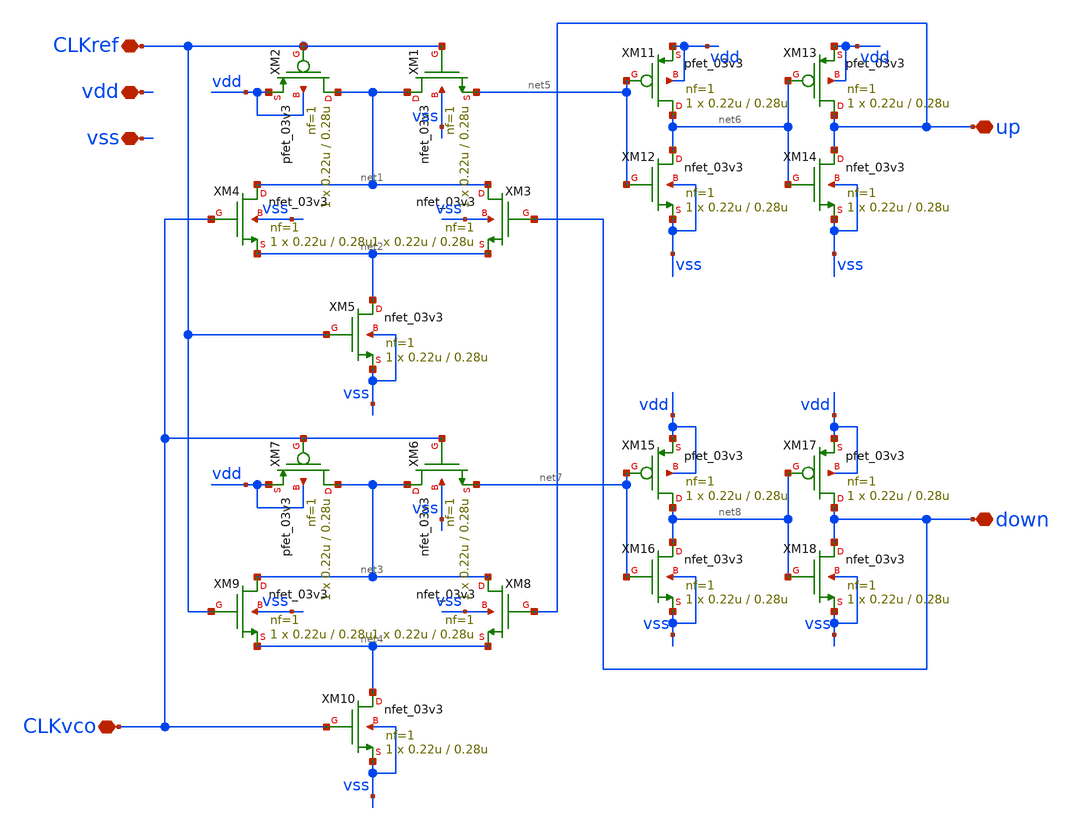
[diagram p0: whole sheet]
** sch_path: designs/libs/qw_core_analog_pkedit/untitled-1.sch
**.subckt untitled-1 CLKref CLKvco vdd vss up down
*.iopin CLKref
*.iopin CLKvco
*.iopin vdd
*.iopin vss
*.iopin up
*.iopin down
XM1 net1 CLKref net5 vss nfet_03v3 L=0.28u W=0.22u nf=1 ad='int((nf+1)/2) * W/nf * 0.18u' as='int((nf+2)/2) * W/nf * 0.18u'
+ pd='2*int((nf+1)/2) * (W/nf + 0.18u)' ps='2*int((nf+2)/2) * (W/nf + 0.18u)' nrd='0.18u / W' nrs='0.18u / W'
+ sa=0 sb=0 sd=0 m=1
XM2 net1 CLKref vdd vdd pfet_03v3 L=0.28u W=0.22u nf=1 ad='int((nf+1)/2) * W/nf * 0.18u' as='int((nf+2)/2) * W/nf * 0.18u'
+ pd='2*int((nf+1)/2) * (W/nf + 0.18u)' ps='2*int((nf+2)/2) * (W/nf + 0.18u)' nrd='0.18u / W' nrs='0.18u / W'
+ sa=0 sb=0 sd=0 m=1
XM3 net1 down net2 vss nfet_03v3 L=0.28u W=0.22u nf=1 ad='int((nf+1)/2) * W/nf * 0.18u' as='int((nf+2)/2) * W/nf * 0.18u'
+ pd='2*int((nf+1)/2) * (W/nf + 0.18u)' ps='2*int((nf+2)/2) * (W/nf + 0.18u)' nrd='0.18u / W' nrs='0.18u / W'
+ sa=0 sb=0 sd=0 m=1
XM4 net1 CLKvco net2 vss nfet_03v3 L=0.28u W=0.22u nf=1 ad='int((nf+1)/2) * W/nf * 0.18u' as='int((nf+2)/2) * W/nf * 0.18u'
+ pd='2*int((nf+1)/2) * (W/nf + 0.18u)' ps='2*int((nf+2)/2) * (W/nf + 0.18u)' nrd='0.18u / W' nrs='0.18u / W'
+ sa=0 sb=0 sd=0 m=1
XM5 net2 CLKref vss vss nfet_03v3 L=0.28u W=0.22u nf=1 ad='int((nf+1)/2) * W/nf * 0.18u' as='int((nf+2)/2) * W/nf * 0.18u'
+ pd='2*int((nf+1)/2) * (W/nf + 0.18u)' ps='2*int((nf+2)/2) * (W/nf + 0.18u)' nrd='0.18u / W' nrs='0.18u / W'
+ sa=0 sb=0 sd=0 m=1
XM6 net3 CLKvco net7 vss nfet_03v3 L=0.28u W=0.22u nf=1 ad='int((nf+1)/2) * W/nf * 0.18u' as='int((nf+2)/2) * W/nf * 0.18u'
+ pd='2*int((nf+1)/2) * (W/nf + 0.18u)' ps='2*int((nf+2)/2) * (W/nf + 0.18u)' nrd='0.18u / W' nrs='0.18u / W'
+ sa=0 sb=0 sd=0 m=1
XM7 net3 CLKvco vdd vdd pfet_03v3 L=0.28u W=0.22u nf=1 ad='int((nf+1)/2) * W/nf * 0.18u' as='int((nf+2)/2) * W/nf * 0.18u'
+ pd='2*int((nf+1)/2) * (W/nf + 0.18u)' ps='2*int((nf+2)/2) * (W/nf + 0.18u)' nrd='0.18u / W' nrs='0.18u / W'
+ sa=0 sb=0 sd=0 m=1
XM8 net3 up net4 vss nfet_03v3 L=0.28u W=0.22u nf=1 ad='int((nf+1)/2) * W/nf * 0.18u' as='int((nf+2)/2) * W/nf * 0.18u'
+ pd='2*int((nf+1)/2) * (W/nf + 0.18u)' ps='2*int((nf+2)/2) * (W/nf + 0.18u)' nrd='0.18u / W' nrs='0.18u / W'
+ sa=0 sb=0 sd=0 m=1
XM9 net3 CLKref net4 vss nfet_03v3 L=0.28u W=0.22u nf=1 ad='int((nf+1)/2) * W/nf * 0.18u' as='int((nf+2)/2) * W/nf * 0.18u'
+ pd='2*int((nf+1)/2) * (W/nf + 0.18u)' ps='2*int((nf+2)/2) * (W/nf + 0.18u)' nrd='0.18u / W' nrs='0.18u / W'
+ sa=0 sb=0 sd=0 m=1
XM10 net4 CLKvco vss vss nfet_03v3 L=0.28u W=0.22u nf=1 ad='int((nf+1)/2) * W/nf * 0.18u' as='int((nf+2)/2) * W/nf * 0.18u'
+ pd='2*int((nf+1)/2) * (W/nf + 0.18u)' ps='2*int((nf+2)/2) * (W/nf + 0.18u)' nrd='0.18u / W' nrs='0.18u / W'
+ sa=0 sb=0 sd=0 m=1
XM11 net6 net5 vdd vdd pfet_03v3 L=0.28u W=0.22u nf=1 ad='int((nf+1)/2) * W/nf * 0.18u' as='int((nf+2)/2) * W/nf * 0.18u'
+ pd='2*int((nf+1)/2) * (W/nf + 0.18u)' ps='2*int((nf+2)/2) * (W/nf + 0.18u)' nrd='0.18u / W' nrs='0.18u / W'
+ sa=0 sb=0 sd=0 m=1
XM12 net6 net5 vss vss nfet_03v3 L=0.28u W=0.22u nf=1 ad='int((nf+1)/2) * W/nf * 0.18u' as='int((nf+2)/2) * W/nf * 0.18u'
+ pd='2*int((nf+1)/2) * (W/nf + 0.18u)' ps='2*int((nf+2)/2) * (W/nf + 0.18u)' nrd='0.18u / W' nrs='0.18u / W'
+ sa=0 sb=0 sd=0 m=1
XM13 up net6 vdd vdd pfet_03v3 L=0.28u W=0.22u nf=1 ad='int((nf+1)/2) * W/nf * 0.18u' as='int((nf+2)/2) * W/nf * 0.18u'
+ pd='2*int((nf+1)/2) * (W/nf + 0.18u)' ps='2*int((nf+2)/2) * (W/nf + 0.18u)' nrd='0.18u / W' nrs='0.18u / W'
+ sa=0 sb=0 sd=0 m=1
XM14 up net6 vss vss nfet_03v3 L=0.28u W=0.22u nf=1 ad='int((nf+1)/2) * W/nf * 0.18u' as='int((nf+2)/2) * W/nf * 0.18u'
+ pd='2*int((nf+1)/2) * (W/nf + 0.18u)' ps='2*int((nf+2)/2) * (W/nf + 0.18u)' nrd='0.18u / W' nrs='0.18u / W'
+ sa=0 sb=0 sd=0 m=1
XM15 net8 net7 vdd vdd pfet_03v3 L=0.28u W=0.22u nf=1 ad='int((nf+1)/2) * W/nf * 0.18u' as='int((nf+2)/2) * W/nf * 0.18u'
+ pd='2*int((nf+1)/2) * (W/nf + 0.18u)' ps='2*int((nf+2)/2) * (W/nf + 0.18u)' nrd='0.18u / W' nrs='0.18u / W'
+ sa=0 sb=0 sd=0 m=1
XM16 net8 net7 vss vss nfet_03v3 L=0.28u W=0.22u nf=1 ad='int((nf+1)/2) * W/nf * 0.18u' as='int((nf+2)/2) * W/nf * 0.18u'
+ pd='2*int((nf+1)/2) * (W/nf + 0.18u)' ps='2*int((nf+2)/2) * (W/nf + 0.18u)' nrd='0.18u / W' nrs='0.18u / W'
+ sa=0 sb=0 sd=0 m=1
XM17 down net8 vdd vdd pfet_03v3 L=0.28u W=0.22u nf=1 ad='int((nf+1)/2) * W/nf * 0.18u' as='int((nf+2)/2) * W/nf * 0.18u'
+ pd='2*int((nf+1)/2) * (W/nf + 0.18u)' ps='2*int((nf+2)/2) * (W/nf + 0.18u)' nrd='0.18u / W' nrs='0.18u / W'
+ sa=0 sb=0 sd=0 m=1
XM18 down net8 vss vss nfet_03v3 L=0.28u W=0.22u nf=1 ad='int((nf+1)/2) * W/nf * 0.18u' as='int((nf+2)/2) * W/nf * 0.18u'
+ pd='2*int((nf+1)/2) * (W/nf + 0.18u)' ps='2*int((nf+2)/2) * (W/nf + 0.18u)' nrd='0.18u / W' nrs='0.18u / W'
+ sa=0 sb=0 sd=0 m=1
**.ends
.end
